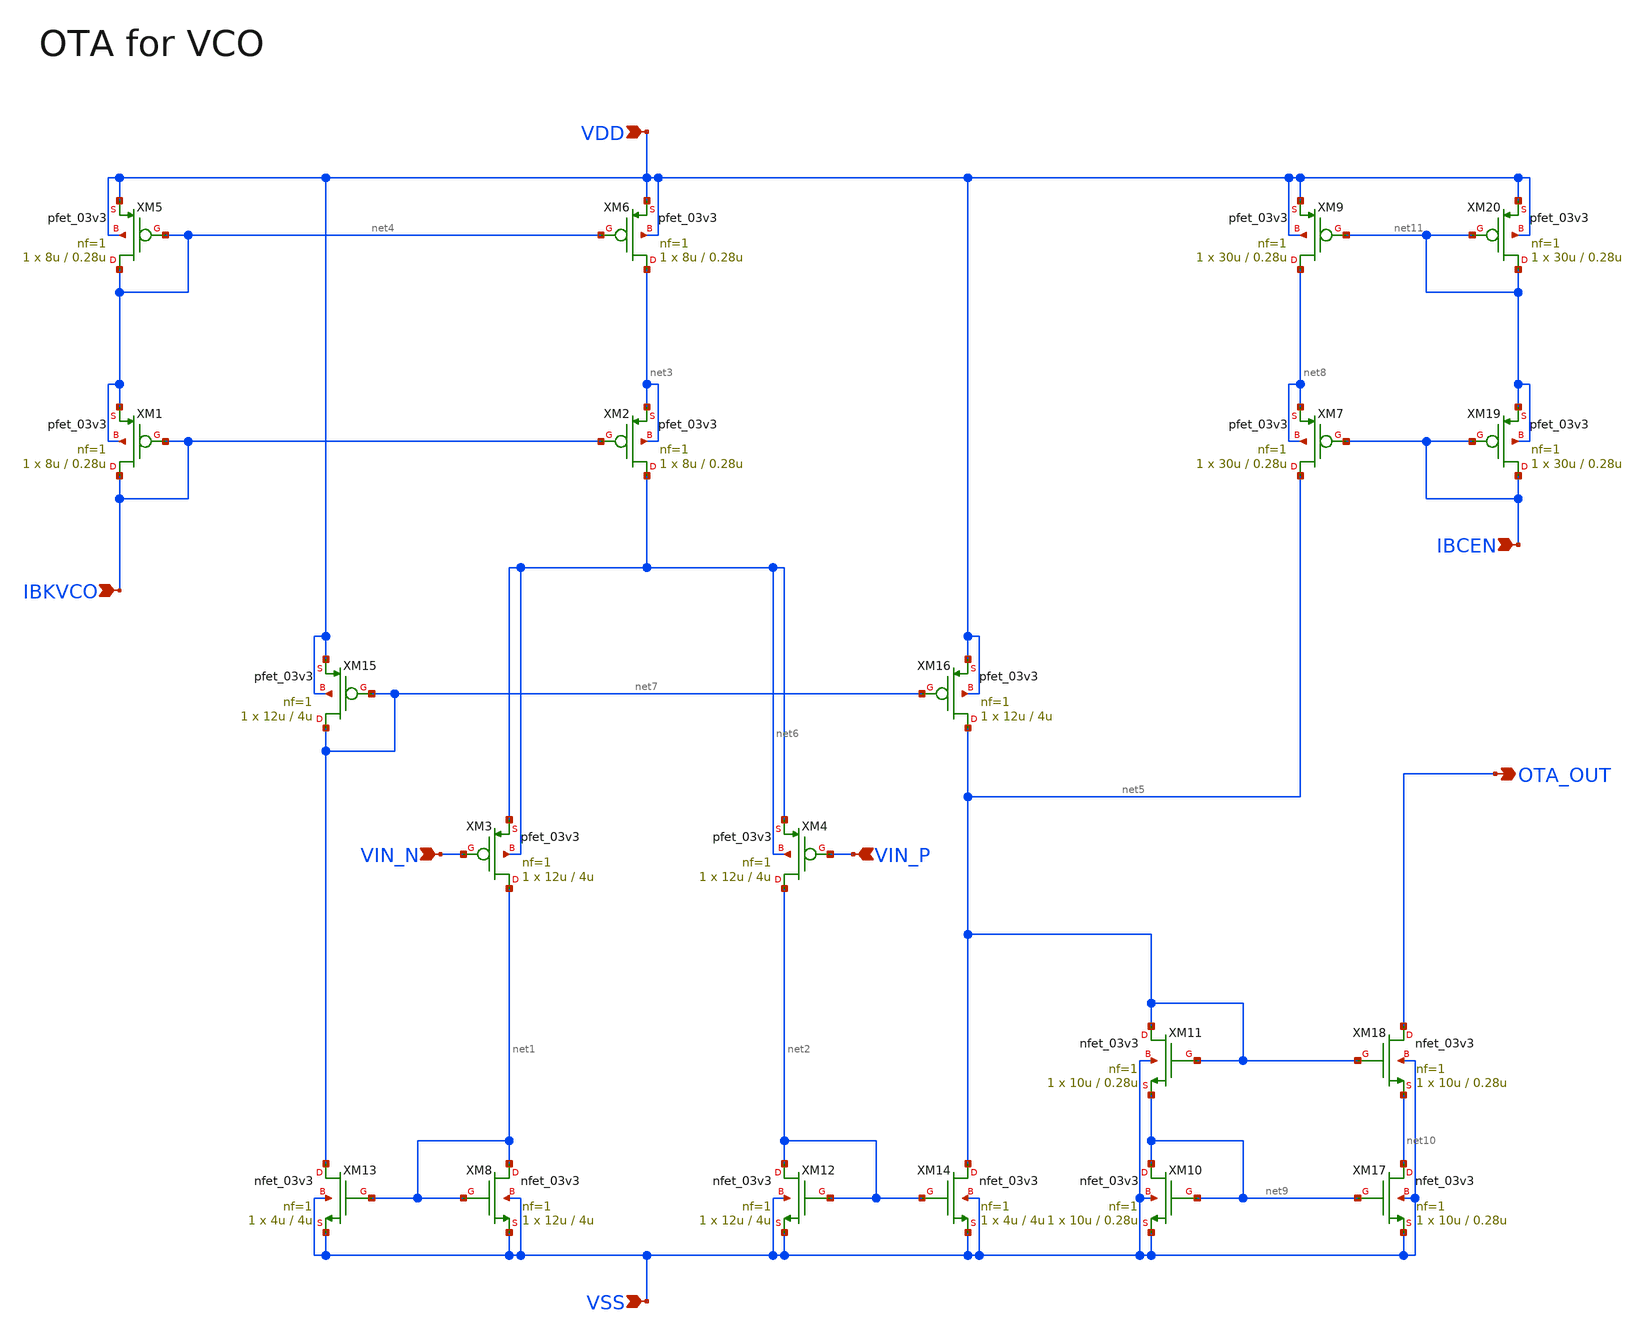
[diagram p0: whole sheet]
** sch_path: designs/libs/core_analog/ota_for_vco/ota_for_vco.sch
**.subckt ota_for_vco IBKVCO VIN_N VIN_P OTA_OUT VSS VDD IBCEN
*.ipin IBKVCO
*.ipin VIN_N
*.ipin VIN_P
*.opin OTA_OUT
*.ipin VSS
*.ipin VDD
*.ipin IBCEN
XM1 IBKVCO IBKVCO net4 net4 pfet_03v3 L=0.28u W=8u nf=1 ad='int((nf+1)/2) * W/nf * 0.18u' as='int((nf+2)/2) * W/nf * 0.18u'
+ pd='2*int((nf+1)/2) * (W/nf + 0.18u)' ps='2*int((nf+2)/2) * (W/nf + 0.18u)' nrd='0.18u / W' nrs='0.18u / W'
+ sa=0 sb=0 sd=0 m=1
XM2 net6 IBKVCO net3 net3 pfet_03v3 L=0.28u W=8u nf=1 ad='int((nf+1)/2) * W/nf * 0.18u' as='int((nf+2)/2) * W/nf * 0.18u'
+ pd='2*int((nf+1)/2) * (W/nf + 0.18u)' ps='2*int((nf+2)/2) * (W/nf + 0.18u)' nrd='0.18u / W' nrs='0.18u / W'
+ sa=0 sb=0 sd=0 m=1
XM3 net1 VIN_N net6 net6 pfet_03v3 L=4u W=12u nf=1 ad='int((nf+1)/2) * W/nf * 0.18u' as='int((nf+2)/2) * W/nf * 0.18u'
+ pd='2*int((nf+1)/2) * (W/nf + 0.18u)' ps='2*int((nf+2)/2) * (W/nf + 0.18u)' nrd='0.18u / W' nrs='0.18u / W'
+ sa=0 sb=0 sd=0 m=1
XM4 net2 VIN_P net6 net6 pfet_03v3 L=4u W=12u nf=1 ad='int((nf+1)/2) * W/nf * 0.18u' as='int((nf+2)/2) * W/nf * 0.18u'
+ pd='2*int((nf+1)/2) * (W/nf + 0.18u)' ps='2*int((nf+2)/2) * (W/nf + 0.18u)' nrd='0.18u / W' nrs='0.18u / W'
+ sa=0 sb=0 sd=0 m=1
XM8 net1 net1 VSS VSS nfet_03v3 L=4u W=12u nf=1 ad='int((nf+1)/2) * W/nf * 0.18u' as='int((nf+2)/2) * W/nf * 0.18u'
+ pd='2*int((nf+1)/2) * (W/nf + 0.18u)' ps='2*int((nf+2)/2) * (W/nf + 0.18u)' nrd='0.18u / W' nrs='0.18u / W'
+ sa=0 sb=0 sd=0 m=1
XM12 net2 net2 VSS VSS nfet_03v3 L=4u W=12u nf=1 ad='int((nf+1)/2) * W/nf * 0.18u' as='int((nf+2)/2) * W/nf * 0.18u'
+ pd='2*int((nf+1)/2) * (W/nf + 0.18u)' ps='2*int((nf+2)/2) * (W/nf + 0.18u)' nrd='0.18u / W' nrs='0.18u / W'
+ sa=0 sb=0 sd=0 m=1
XM13 net7 net1 VSS VSS nfet_03v3 L=4u W=4u nf=1 ad='int((nf+1)/2) * W/nf * 0.18u' as='int((nf+2)/2) * W/nf * 0.18u'
+ pd='2*int((nf+1)/2) * (W/nf + 0.18u)' ps='2*int((nf+2)/2) * (W/nf + 0.18u)' nrd='0.18u / W' nrs='0.18u / W'
+ sa=0 sb=0 sd=0 m=1
XM14 net5 net2 VSS VSS nfet_03v3 L=4u W=4u nf=1 ad='int((nf+1)/2) * W/nf * 0.18u' as='int((nf+2)/2) * W/nf * 0.18u'
+ pd='2*int((nf+1)/2) * (W/nf + 0.18u)' ps='2*int((nf+2)/2) * (W/nf + 0.18u)' nrd='0.18u / W' nrs='0.18u / W'
+ sa=0 sb=0 sd=0 m=1
XM15 net7 net7 VDD VDD pfet_03v3 L=4u W=12u nf=1 ad='int((nf+1)/2) * W/nf * 0.18u' as='int((nf+2)/2) * W/nf * 0.18u'
+ pd='2*int((nf+1)/2) * (W/nf + 0.18u)' ps='2*int((nf+2)/2) * (W/nf + 0.18u)' nrd='0.18u / W' nrs='0.18u / W'
+ sa=0 sb=0 sd=0 m=1
XM16 net5 net7 VDD VDD pfet_03v3 L=4u W=12u nf=1 ad='int((nf+1)/2) * W/nf * 0.18u' as='int((nf+2)/2) * W/nf * 0.18u'
+ pd='2*int((nf+1)/2) * (W/nf + 0.18u)' ps='2*int((nf+2)/2) * (W/nf + 0.18u)' nrd='0.18u / W' nrs='0.18u / W'
+ sa=0 sb=0 sd=0 m=1
XM5 net4 net4 VDD VDD pfet_03v3 L=0.28u W=8u nf=1 ad='int((nf+1)/2) * W/nf * 0.18u' as='int((nf+2)/2) * W/nf * 0.18u'
+ pd='2*int((nf+1)/2) * (W/nf + 0.18u)' ps='2*int((nf+2)/2) * (W/nf + 0.18u)' nrd='0.18u / W' nrs='0.18u / W'
+ sa=0 sb=0 sd=0 m=1
XM6 net3 net4 VDD VDD pfet_03v3 L=0.28u W=8u nf=1 ad='int((nf+1)/2) * W/nf * 0.18u' as='int((nf+2)/2) * W/nf * 0.18u'
+ pd='2*int((nf+1)/2) * (W/nf + 0.18u)' ps='2*int((nf+2)/2) * (W/nf + 0.18u)' nrd='0.18u / W' nrs='0.18u / W'
+ sa=0 sb=0 sd=0 m=1
XM7 net5 IBCEN net8 net8 pfet_03v3 L=0.28u W=30u nf=1 ad='int((nf+1)/2) * W/nf * 0.18u' as='int((nf+2)/2) * W/nf * 0.18u'
+ pd='2*int((nf+1)/2) * (W/nf + 0.18u)' ps='2*int((nf+2)/2) * (W/nf + 0.18u)' nrd='0.18u / W' nrs='0.18u / W'
+ sa=0 sb=0 sd=0 m=1
XM9 net8 net11 VDD VDD pfet_03v3 L=0.28u W=30u nf=1 ad='int((nf+1)/2) * W/nf * 0.18u' as='int((nf+2)/2) * W/nf * 0.18u'
+ pd='2*int((nf+1)/2) * (W/nf + 0.18u)' ps='2*int((nf+2)/2) * (W/nf + 0.18u)' nrd='0.18u / W' nrs='0.18u / W'
+ sa=0 sb=0 sd=0 m=1
XM10 net9 net9 VSS VSS nfet_03v3 L=0.28u W=10u nf=1 ad='int((nf+1)/2) * W/nf * 0.18u' as='int((nf+2)/2) * W/nf * 0.18u'
+ pd='2*int((nf+1)/2) * (W/nf + 0.18u)' ps='2*int((nf+2)/2) * (W/nf + 0.18u)' nrd='0.18u / W' nrs='0.18u / W'
+ sa=0 sb=0 sd=0 m=1
XM17 net10 net9 VSS VSS nfet_03v3 L=0.28u W=10u nf=1 ad='int((nf+1)/2) * W/nf * 0.18u' as='int((nf+2)/2) * W/nf * 0.18u'
+ pd='2*int((nf+1)/2) * (W/nf + 0.18u)' ps='2*int((nf+2)/2) * (W/nf + 0.18u)' nrd='0.18u / W' nrs='0.18u / W'
+ sa=0 sb=0 sd=0 m=1
XM19 IBCEN IBCEN net11 net11 pfet_03v3 L=0.28u W=30u nf=1 ad='int((nf+1)/2) * W/nf * 0.18u' as='int((nf+2)/2) * W/nf * 0.18u'
+ pd='2*int((nf+1)/2) * (W/nf + 0.18u)' ps='2*int((nf+2)/2) * (W/nf + 0.18u)' nrd='0.18u / W' nrs='0.18u / W'
+ sa=0 sb=0 sd=0 m=1
XM20 net11 net11 VDD VDD pfet_03v3 L=0.28u W=30u nf=1 ad='int((nf+1)/2) * W/nf * 0.18u' as='int((nf+2)/2) * W/nf * 0.18u'
+ pd='2*int((nf+1)/2) * (W/nf + 0.18u)' ps='2*int((nf+2)/2) * (W/nf + 0.18u)' nrd='0.18u / W' nrs='0.18u / W'
+ sa=0 sb=0 sd=0 m=1
XM11 net5 net5 net9 VSS nfet_03v3 L=0.28u W=10u nf=1 ad='int((nf+1)/2) * W/nf * 0.18u' as='int((nf+2)/2) * W/nf * 0.18u'
+ pd='2*int((nf+1)/2) * (W/nf + 0.18u)' ps='2*int((nf+2)/2) * (W/nf + 0.18u)' nrd='0.18u / W' nrs='0.18u / W'
+ sa=0 sb=0 sd=0 m=1
XM18 OTA_OUT net5 net10 VSS nfet_03v3 L=0.28u W=10u nf=1 ad='int((nf+1)/2) * W/nf * 0.18u' as='int((nf+2)/2) * W/nf * 0.18u'
+ pd='2*int((nf+1)/2) * (W/nf + 0.18u)' ps='2*int((nf+2)/2) * (W/nf + 0.18u)' nrd='0.18u / W' nrs='0.18u / W'
+ sa=0 sb=0 sd=0 m=1
**.ends
.end
